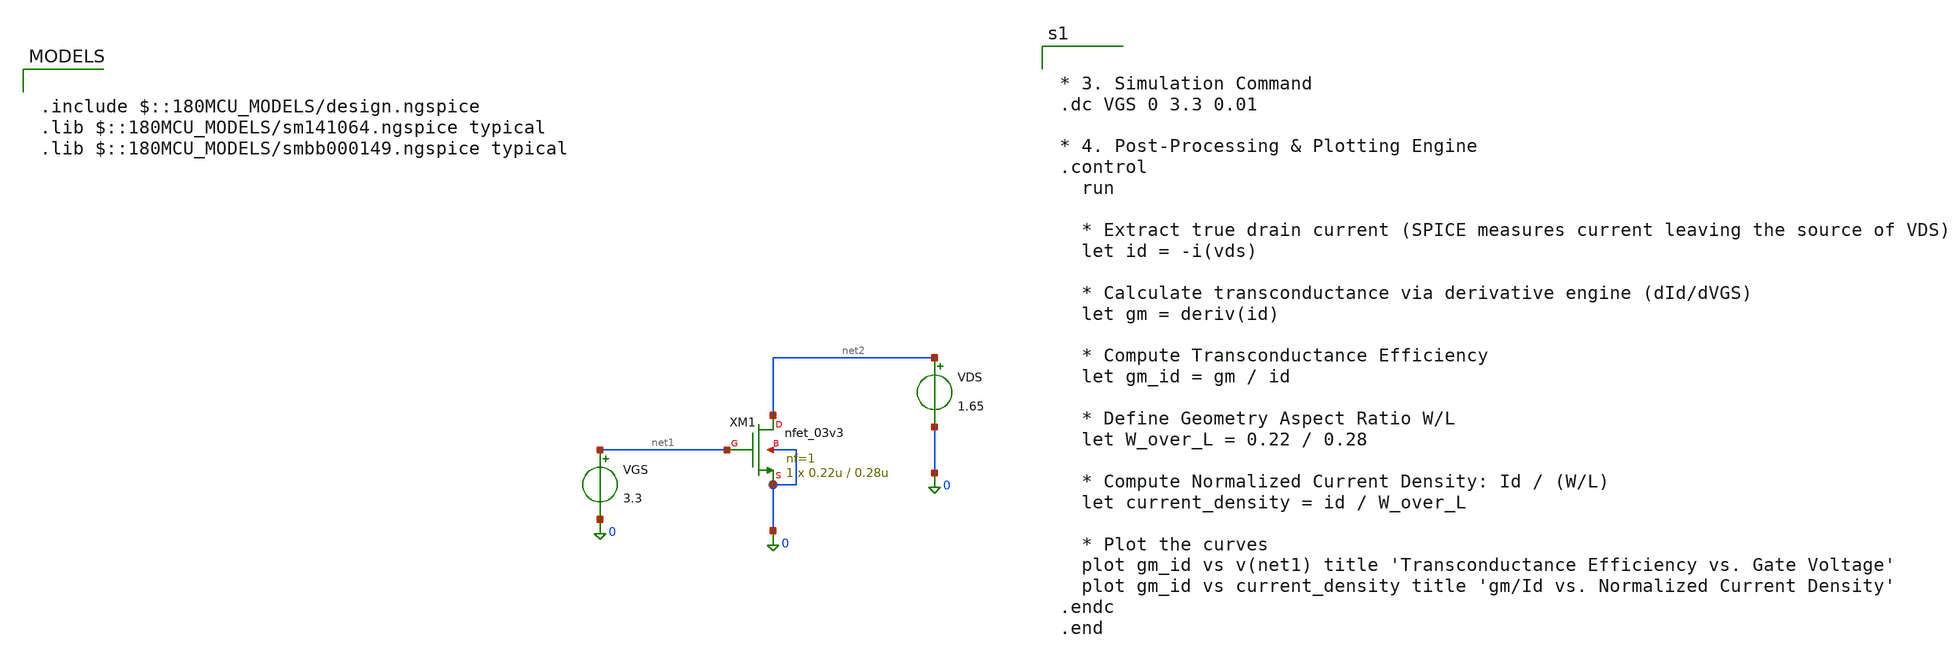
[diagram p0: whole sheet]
** sch_path: analog/blocks/Double_Tail_Comparator/transistest.sch
**.subckt transistest
VGS net1 0 3.3
VDS net2 0 1.65
XM1 net2 net1 0 0 nfet_03v3 L=0.28u W=0.22u nf=1 ad='int((nf+1)/2) * W/nf * 0.18u' as='int((nf+2)/2) * W/nf * 0.18u'
+ pd='2*int((nf+1)/2) * (W/nf + 0.18u)' ps='2*int((nf+2)/2) * (W/nf + 0.18u)' nrd='0.18u / W' nrs='0.18u / W'
+ sa=0 sb=0 sd=0 m=1
**** begin user architecture code

.include $::180MCU_MODELS/design.ngspice
.lib $::180MCU_MODELS/sm141064.ngspice typical
.lib $::180MCU_MODELS/smbb000149.ngspice typical



* 3. Simulation Command
.dc VGS 0 3.3 0.01

* 4. Post-Processing & Plotting Engine
.control
  run

  * Extract true drain current (SPICE measures current leaving the source of VDS)
  let id = -i(vds)

  * Calculate transconductance via derivative engine (dId/dVGS)
  let gm = deriv(id)

  * Compute Transconductance Efficiency
  let gm_id = gm / id

  * Define Geometry Aspect Ratio W/L
  let W_over_L = 0.22 / 0.28

  * Compute Normalized Current Density: Id / (W/L)
  let current_density = id / W_over_L

  * Plot the curves
  plot gm_id vs v(net1) title 'Transconductance Efficiency vs. Gate Voltage'
  plot gm_id vs current_density title 'gm/Id vs. Normalized Current Density'
.endc
.end


**** end user architecture code
**.ends
.end
